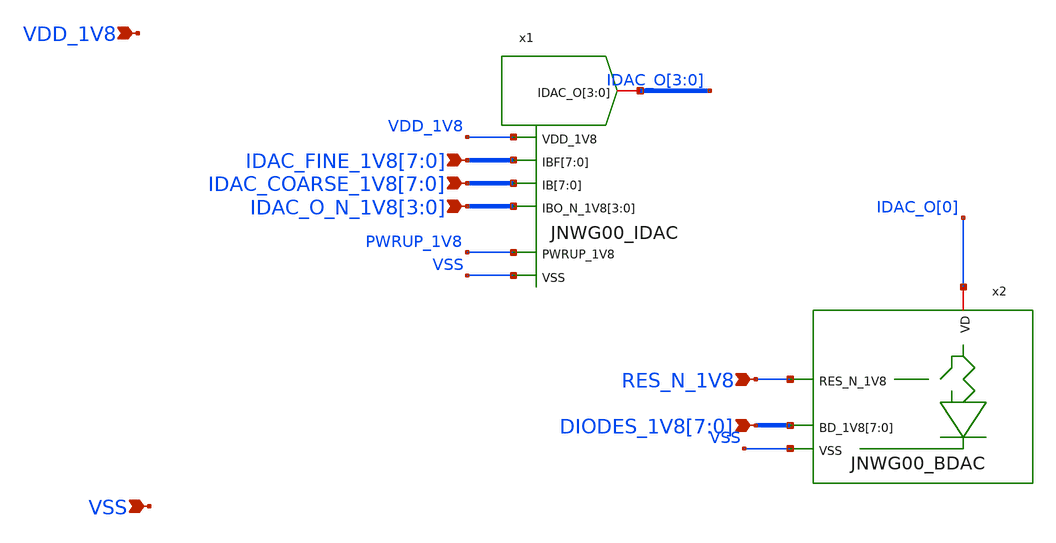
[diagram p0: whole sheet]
** sch_path: design/JNW_GR00_SKY130NM/JNWG00_CORE.sch
**.subckt JNWG00_CORE VDD_1V8 VSS
*+ IDAC_FINE_1V8[7],IDAC_FINE_1V8[6],IDAC_FINE_1V8[5],IDAC_FINE_1V8[4],IDAC_FINE_1V8[3],IDAC_FINE_1V8[2],IDAC_FINE_1V8[1],IDAC_FINE_1V8[0]
*+ IDAC_COARSE_1V8[7],IDAC_COARSE_1V8[6],IDAC_COARSE_1V8[5],IDAC_COARSE_1V8[4],IDAC_COARSE_1V8[3],IDAC_COARSE_1V8[2],IDAC_COARSE_1V8[1],IDAC_COARSE_1V8[0] IDAC_O_N_1V8[3],IDAC_O_N_1V8[2],IDAC_O_N_1V8[1],IDAC_O_N_1V8[0] RES_N_1V8
*+ DIODES_1V8[7],DIODES_1V8[6],DIODES_1V8[5],DIODES_1V8[4],DIODES_1V8[3],DIODES_1V8[2],DIODES_1V8[1],DIODES_1V8[0]
*.ipin VDD_1V8
*.ipin VSS
*.ipin
*+ IDAC_FINE_1V8[7],IDAC_FINE_1V8[6],IDAC_FINE_1V8[5],IDAC_FINE_1V8[4],IDAC_FINE_1V8[3],IDAC_FINE_1V8[2],IDAC_FINE_1V8[1],IDAC_FINE_1V8[0]
*.ipin
*+ IDAC_COARSE_1V8[7],IDAC_COARSE_1V8[6],IDAC_COARSE_1V8[5],IDAC_COARSE_1V8[4],IDAC_COARSE_1V8[3],IDAC_COARSE_1V8[2],IDAC_COARSE_1V8[1],IDAC_COARSE_1V8[0]
*.ipin IDAC_O_N_1V8[3],IDAC_O_N_1V8[2],IDAC_O_N_1V8[1],IDAC_O_N_1V8[0]
*.ipin RES_N_1V8
*.ipin
*+ DIODES_1V8[7],DIODES_1V8[6],DIODES_1V8[5],DIODES_1V8[4],DIODES_1V8[3],DIODES_1V8[2],DIODES_1V8[1],DIODES_1V8[0]
x2 DIODES_1V8[7] DIODES_1V8[6] DIODES_1V8[5] DIODES_1V8[4] DIODES_1V8[3] DIODES_1V8[2] DIODES_1V8[1]
+ DIODES_1V8[0] IDAC_O[0] VSS RES_N_1V8 JNWG00_BDAC
x1 IDAC_FINE_1V8[7] IDAC_FINE_1V8[6] IDAC_FINE_1V8[5] IDAC_FINE_1V8[4] IDAC_FINE_1V8[3]
+ IDAC_FINE_1V8[2] IDAC_FINE_1V8[1] IDAC_FINE_1V8[0] IDAC_COARSE_1V8[7] IDAC_COARSE_1V8[6] IDAC_COARSE_1V8[5]
+ IDAC_COARSE_1V8[4] IDAC_COARSE_1V8[3] IDAC_COARSE_1V8[2] IDAC_COARSE_1V8[1] IDAC_COARSE_1V8[0] VDD_1V8 IDAC_O[3]
+ IDAC_O[2] IDAC_O[1] IDAC_O[0] IDAC_O_N_1V8[3] IDAC_O_N_1V8[2] IDAC_O_N_1V8[1] IDAC_O_N_1V8[0] PWRUP_1V8 VSS
+ JNWG00_IDAC
**.ends
.end
